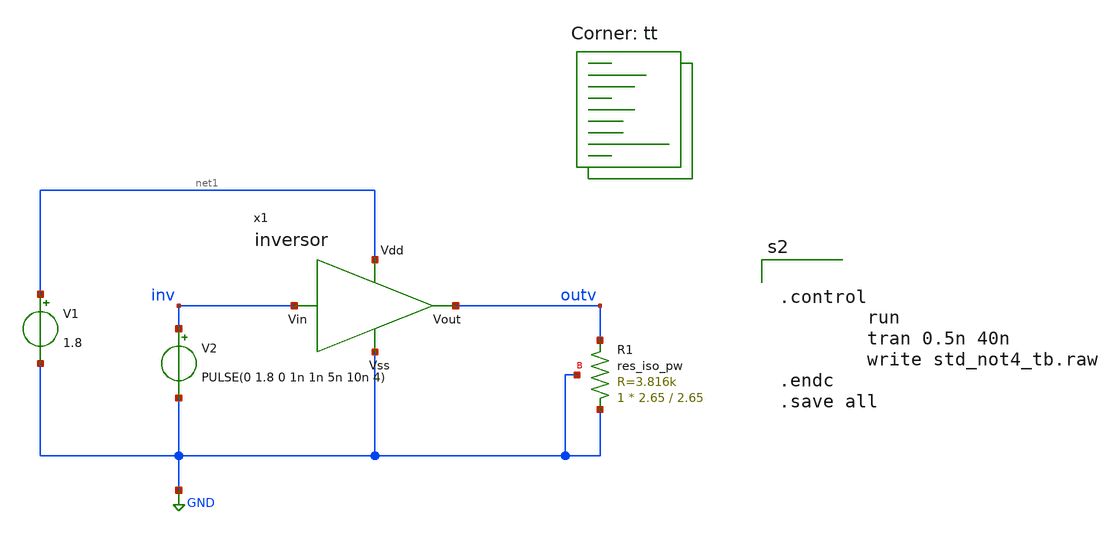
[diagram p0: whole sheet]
** sch_path: trabajosPracticos/tp6/archivosDelProfe/inversor/simulacionnot.sch

**.subckt simulacionnot
V2 inv GND PULSE(0 1.8 0 1n 1n 5n 10n 4)
V1 net1 GND 1.8
XR1 GND outv GND sky130_fd_pr__res_iso_pw W=2.65 L=2.65 m=1
x1 net1 inv outv GND inversor
**** begin user architecture code
.lib $::SKYWATER_MODELS/sky130.lib.spice tt


.control
        run
        tran 0.5n 40n
        write std_not4_tb.raw
.endc
.save all


**** end user architecture code
**.ends

* expanding   symbol:  inversor.sym # of pins=4
** sym_path: trabajosPracticos/tp6/archivosDelProfe/inversor/inversor.sym
** sch_path: trabajosPracticos/tp6/archivosDelProfe/inversor/inversor.sch
.subckt inversor Vdd Vin Vout Vss
*.ipin Vdd
*.ipin Vss
*.ipin Vin
*.opin Vout
XM2 Vout Vin Vdd Vdd sky130_fd_pr__pfet_01v8 L=0.15 W=2.1 nf=1 ad='int((nf+1)/2) * W/nf * 0.29' as='int((nf+2)/2) * W/nf * 0.29'
+ pd='2*int((nf+1)/2) * (W/nf + 0.29)' ps='2*int((nf+2)/2) * (W/nf + 0.29)' nrd='0.29 / W' nrs='0.29 / W'
+ sa=0 sb=0 sd=0 mult=1 m=1
XM1 Vout Vin Vss Vss sky130_fd_pr__nfet_01v8 L=0.15 W=1.05 nf=1 ad='int((nf+1)/2) * W/nf * 0.29' as='int((nf+2)/2) * W/nf * 0.29'
+ pd='2*int((nf+1)/2) * (W/nf + 0.29)' ps='2*int((nf+2)/2) * (W/nf + 0.29)' nrd='0.29 / W' nrs='0.29 / W'
+ sa=0 sb=0 sd=0 mult=1 m=1
.ends

.GLOBAL GND
.end
